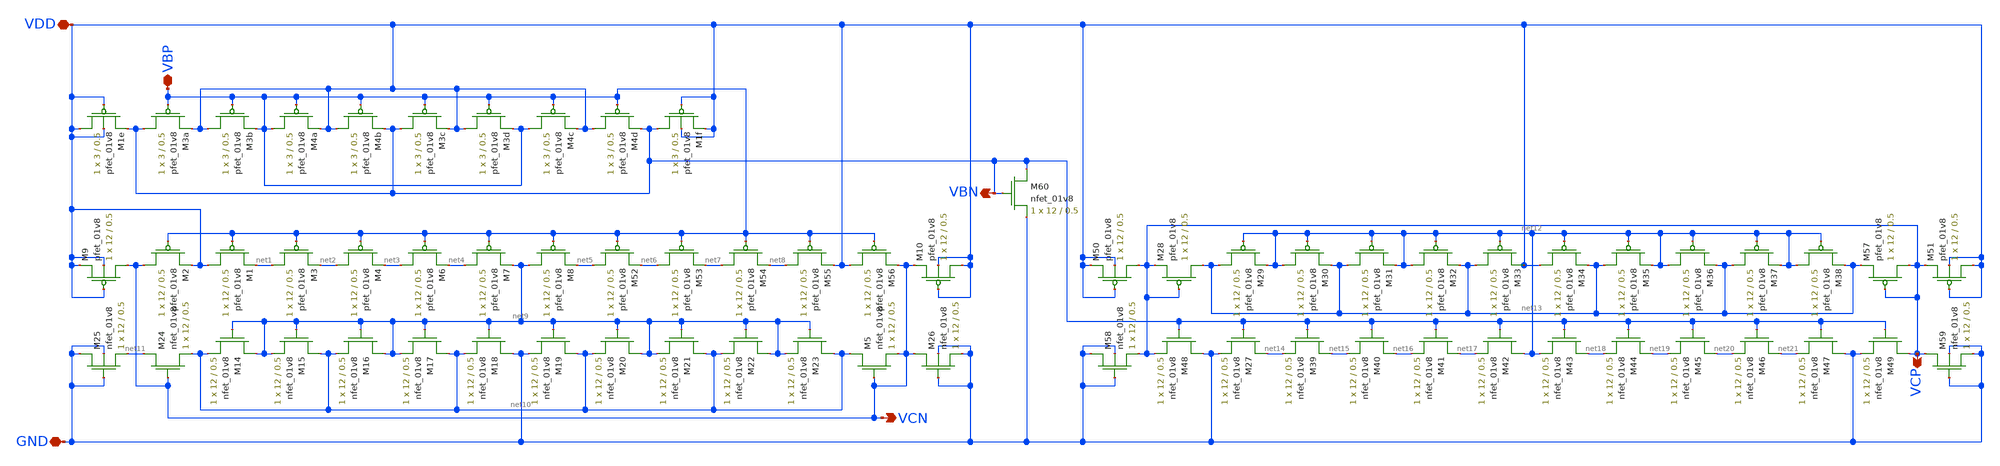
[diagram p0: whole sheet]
** sch_path: mp3/schematics/bias_generator_lds.sch
**.subckt bias_generator_lds VBP VDD GND VCN VCP VBN
*.iopin VBP
*.iopin VDD
*.iopin GND
*.opin VCN
*.opin VCP
*.opin VBN
XM9 VCN VDD VDD VDD sky130_fd_pr__pfet_01v8 L=0.5 W=12 nf=1 ad='int((nf+1)/2) * W/nf * 0.29' as='int((nf+2)/2) * W/nf * 0.29'
+ pd='2*int((nf+1)/2) * (W/nf + 0.29)' ps='2*int((nf+2)/2) * (W/nf + 0.29)' nrd='0.29 / W' nrs='0.29 / W'
+ sa=0 sb=0 sd=0 mult=1 m=1
XM24 net11 VCN net10 GND sky130_fd_pr__nfet_01v8 L=0.5 W=12 nf=1 ad='int((nf+1)/2) * W/nf * 0.29' as='int((nf+2)/2) * W/nf * 0.29'
+ pd='2*int((nf+1)/2) * (W/nf + 0.29)' ps='2*int((nf+2)/2) * (W/nf + 0.29)' nrd='0.29 / W' nrs='0.29 / W'
+ sa=0 sb=0 sd=0 mult=1 m=1
XM2 VCN VBP VDD VDD sky130_fd_pr__pfet_01v8 L=0.5 W=12 nf=1 ad='int((nf+1)/2) * W/nf * 0.29' as='int((nf+2)/2) * W/nf * 0.29'
+ pd='2*int((nf+1)/2) * (W/nf + 0.29)' ps='2*int((nf+2)/2) * (W/nf + 0.29)' nrd='0.29 / W' nrs='0.29 / W'
+ sa=0 sb=0 sd=0 mult=1 m=1
XM1 VDD VBP net1 VDD sky130_fd_pr__pfet_01v8 L=0.5 W=12 nf=1 ad='int((nf+1)/2) * W/nf * 0.29' as='int((nf+2)/2) * W/nf * 0.29'
+ pd='2*int((nf+1)/2) * (W/nf + 0.29)' ps='2*int((nf+2)/2) * (W/nf + 0.29)' nrd='0.29 / W' nrs='0.29 / W'
+ sa=0 sb=0 sd=0 mult=1 m=1
XM3 net1 VBP net2 VDD sky130_fd_pr__pfet_01v8 L=0.5 W=12 nf=1 ad='int((nf+1)/2) * W/nf * 0.29' as='int((nf+2)/2) * W/nf * 0.29'
+ pd='2*int((nf+1)/2) * (W/nf + 0.29)' ps='2*int((nf+2)/2) * (W/nf + 0.29)' nrd='0.29 / W' nrs='0.29 / W'
+ sa=0 sb=0 sd=0 mult=1 m=1
XM4 net2 VBP net3 VDD sky130_fd_pr__pfet_01v8 L=0.5 W=12 nf=1 ad='int((nf+1)/2) * W/nf * 0.29' as='int((nf+2)/2) * W/nf * 0.29'
+ pd='2*int((nf+1)/2) * (W/nf + 0.29)' ps='2*int((nf+2)/2) * (W/nf + 0.29)' nrd='0.29 / W' nrs='0.29 / W'
+ sa=0 sb=0 sd=0 mult=1 m=1
XM6 net3 VBP net4 VDD sky130_fd_pr__pfet_01v8 L=0.5 W=12 nf=1 ad='int((nf+1)/2) * W/nf * 0.29' as='int((nf+2)/2) * W/nf * 0.29'
+ pd='2*int((nf+1)/2) * (W/nf + 0.29)' ps='2*int((nf+2)/2) * (W/nf + 0.29)' nrd='0.29 / W' nrs='0.29 / W'
+ sa=0 sb=0 sd=0 mult=1 m=1
XM7 net4 VBP net9 VDD sky130_fd_pr__pfet_01v8 L=0.5 W=12 nf=1 ad='int((nf+1)/2) * W/nf * 0.29' as='int((nf+2)/2) * W/nf * 0.29'
+ pd='2*int((nf+1)/2) * (W/nf + 0.29)' ps='2*int((nf+2)/2) * (W/nf + 0.29)' nrd='0.29 / W' nrs='0.29 / W'
+ sa=0 sb=0 sd=0 mult=1 m=1
XM8 net9 VBP net5 VDD sky130_fd_pr__pfet_01v8 L=0.5 W=12 nf=1 ad='int((nf+1)/2) * W/nf * 0.29' as='int((nf+2)/2) * W/nf * 0.29'
+ pd='2*int((nf+1)/2) * (W/nf + 0.29)' ps='2*int((nf+2)/2) * (W/nf + 0.29)' nrd='0.29 / W' nrs='0.29 / W'
+ sa=0 sb=0 sd=0 mult=1 m=1
XM52 net5 VBP net6 VDD sky130_fd_pr__pfet_01v8 L=0.5 W=12 nf=1 ad='int((nf+1)/2) * W/nf * 0.29' as='int((nf+2)/2) * W/nf * 0.29'
+ pd='2*int((nf+1)/2) * (W/nf + 0.29)' ps='2*int((nf+2)/2) * (W/nf + 0.29)' nrd='0.29 / W' nrs='0.29 / W'
+ sa=0 sb=0 sd=0 mult=1 m=1
XM53 net6 VBP net7 VDD sky130_fd_pr__pfet_01v8 L=0.5 W=12 nf=1 ad='int((nf+1)/2) * W/nf * 0.29' as='int((nf+2)/2) * W/nf * 0.29'
+ pd='2*int((nf+1)/2) * (W/nf + 0.29)' ps='2*int((nf+2)/2) * (W/nf + 0.29)' nrd='0.29 / W' nrs='0.29 / W'
+ sa=0 sb=0 sd=0 mult=1 m=1
XM54 net7 VBP net8 VDD sky130_fd_pr__pfet_01v8 L=0.5 W=12 nf=1 ad='int((nf+1)/2) * W/nf * 0.29' as='int((nf+2)/2) * W/nf * 0.29'
+ pd='2*int((nf+1)/2) * (W/nf + 0.29)' ps='2*int((nf+2)/2) * (W/nf + 0.29)' nrd='0.29 / W' nrs='0.29 / W'
+ sa=0 sb=0 sd=0 mult=1 m=1
XM55 net8 VBP VDD VDD sky130_fd_pr__pfet_01v8 L=0.5 W=12 nf=1 ad='int((nf+1)/2) * W/nf * 0.29' as='int((nf+2)/2) * W/nf * 0.29'
+ pd='2*int((nf+1)/2) * (W/nf + 0.29)' ps='2*int((nf+2)/2) * (W/nf + 0.29)' nrd='0.29 / W' nrs='0.29 / W'
+ sa=0 sb=0 sd=0 mult=1 m=1
XM56 VDD VBP VCN VDD sky130_fd_pr__pfet_01v8 L=0.5 W=12 nf=1 ad='int((nf+1)/2) * W/nf * 0.29' as='int((nf+2)/2) * W/nf * 0.29'
+ pd='2*int((nf+1)/2) * (W/nf + 0.29)' ps='2*int((nf+2)/2) * (W/nf + 0.29)' nrd='0.29 / W' nrs='0.29 / W'
+ sa=0 sb=0 sd=0 mult=1 m=1
XM10 VDD VDD VCN VDD sky130_fd_pr__pfet_01v8 L=0.5 W=12 nf=1 ad='int((nf+1)/2) * W/nf * 0.29' as='int((nf+2)/2) * W/nf * 0.29'
+ pd='2*int((nf+1)/2) * (W/nf + 0.29)' ps='2*int((nf+2)/2) * (W/nf + 0.29)' nrd='0.29 / W' nrs='0.29 / W'
+ sa=0 sb=0 sd=0 mult=1 m=1
XM25 GND GND net11 GND sky130_fd_pr__nfet_01v8 L=0.5 W=12 nf=1 ad='int((nf+1)/2) * W/nf * 0.29' as='int((nf+2)/2) * W/nf * 0.29'
+ pd='2*int((nf+1)/2) * (W/nf + 0.29)' ps='2*int((nf+2)/2) * (W/nf + 0.29)' nrd='0.29 / W' nrs='0.29 / W'
+ sa=0 sb=0 sd=0 mult=1 m=1
XM14 net9 net9 net10 GND sky130_fd_pr__nfet_01v8 L=0.5 W=12 nf=1 ad='int((nf+1)/2) * W/nf * 0.29' as='int((nf+2)/2) * W/nf * 0.29'
+ pd='2*int((nf+1)/2) * (W/nf + 0.29)' ps='2*int((nf+2)/2) * (W/nf + 0.29)' nrd='0.29 / W' nrs='0.29 / W'
+ sa=0 sb=0 sd=0 mult=1 m=1
XM15 net10 net9 net9 GND sky130_fd_pr__nfet_01v8 L=0.5 W=12 nf=1 ad='int((nf+1)/2) * W/nf * 0.29' as='int((nf+2)/2) * W/nf * 0.29'
+ pd='2*int((nf+1)/2) * (W/nf + 0.29)' ps='2*int((nf+2)/2) * (W/nf + 0.29)' nrd='0.29 / W' nrs='0.29 / W'
+ sa=0 sb=0 sd=0 mult=1 m=1
XM16 net9 net9 net10 GND sky130_fd_pr__nfet_01v8 L=0.5 W=12 nf=1 ad='int((nf+1)/2) * W/nf * 0.29' as='int((nf+2)/2) * W/nf * 0.29'
+ pd='2*int((nf+1)/2) * (W/nf + 0.29)' ps='2*int((nf+2)/2) * (W/nf + 0.29)' nrd='0.29 / W' nrs='0.29 / W'
+ sa=0 sb=0 sd=0 mult=1 m=1
XM17 net10 net9 net9 GND sky130_fd_pr__nfet_01v8 L=0.5 W=12 nf=1 ad='int((nf+1)/2) * W/nf * 0.29' as='int((nf+2)/2) * W/nf * 0.29'
+ pd='2*int((nf+1)/2) * (W/nf + 0.29)' ps='2*int((nf+2)/2) * (W/nf + 0.29)' nrd='0.29 / W' nrs='0.29 / W'
+ sa=0 sb=0 sd=0 mult=1 m=1
XM18 GND net9 net10 GND sky130_fd_pr__nfet_01v8 L=0.5 W=12 nf=1 ad='int((nf+1)/2) * W/nf * 0.29' as='int((nf+2)/2) * W/nf * 0.29'
+ pd='2*int((nf+1)/2) * (W/nf + 0.29)' ps='2*int((nf+2)/2) * (W/nf + 0.29)' nrd='0.29 / W' nrs='0.29 / W'
+ sa=0 sb=0 sd=0 mult=1 m=1
XM19 net10 net9 GND GND sky130_fd_pr__nfet_01v8 L=0.5 W=12 nf=1 ad='int((nf+1)/2) * W/nf * 0.29' as='int((nf+2)/2) * W/nf * 0.29'
+ pd='2*int((nf+1)/2) * (W/nf + 0.29)' ps='2*int((nf+2)/2) * (W/nf + 0.29)' nrd='0.29 / W' nrs='0.29 / W'
+ sa=0 sb=0 sd=0 mult=1 m=1
XM20 net9 net9 net10 GND sky130_fd_pr__nfet_01v8 L=0.5 W=12 nf=1 ad='int((nf+1)/2) * W/nf * 0.29' as='int((nf+2)/2) * W/nf * 0.29'
+ pd='2*int((nf+1)/2) * (W/nf + 0.29)' ps='2*int((nf+2)/2) * (W/nf + 0.29)' nrd='0.29 / W' nrs='0.29 / W'
+ sa=0 sb=0 sd=0 mult=1 m=1
XM21 net10 net9 net9 GND sky130_fd_pr__nfet_01v8 L=0.5 W=12 nf=1 ad='int((nf+1)/2) * W/nf * 0.29' as='int((nf+2)/2) * W/nf * 0.29'
+ pd='2*int((nf+1)/2) * (W/nf + 0.29)' ps='2*int((nf+2)/2) * (W/nf + 0.29)' nrd='0.29 / W' nrs='0.29 / W'
+ sa=0 sb=0 sd=0 mult=1 m=1
XM22 net9 net9 net10 GND sky130_fd_pr__nfet_01v8 L=0.5 W=12 nf=1 ad='int((nf+1)/2) * W/nf * 0.29' as='int((nf+2)/2) * W/nf * 0.29'
+ pd='2*int((nf+1)/2) * (W/nf + 0.29)' ps='2*int((nf+2)/2) * (W/nf + 0.29)' nrd='0.29 / W' nrs='0.29 / W'
+ sa=0 sb=0 sd=0 mult=1 m=1
XM23 net10 net9 net9 GND sky130_fd_pr__nfet_01v8 L=0.5 W=12 nf=1 ad='int((nf+1)/2) * W/nf * 0.29' as='int((nf+2)/2) * W/nf * 0.29'
+ pd='2*int((nf+1)/2) * (W/nf + 0.29)' ps='2*int((nf+2)/2) * (W/nf + 0.29)' nrd='0.29 / W' nrs='0.29 / W'
+ sa=0 sb=0 sd=0 mult=1 m=1
XM5 net10 VCN VCN GND sky130_fd_pr__nfet_01v8 L=0.5 W=12 nf=1 ad='int((nf+1)/2) * W/nf * 0.29' as='int((nf+2)/2) * W/nf * 0.29'
+ pd='2*int((nf+1)/2) * (W/nf + 0.29)' ps='2*int((nf+2)/2) * (W/nf + 0.29)' nrd='0.29 / W' nrs='0.29 / W'
+ sa=0 sb=0 sd=0 mult=1 m=1
XM26 VCN GND GND GND sky130_fd_pr__nfet_01v8 L=0.5 W=12 nf=1 ad='int((nf+1)/2) * W/nf * 0.29' as='int((nf+2)/2) * W/nf * 0.29'
+ pd='2*int((nf+1)/2) * (W/nf + 0.29)' ps='2*int((nf+2)/2) * (W/nf + 0.29)' nrd='0.29 / W' nrs='0.29 / W'
+ sa=0 sb=0 sd=0 mult=1 m=1
XM27 net14 VBN GND GND sky130_fd_pr__nfet_01v8 L=0.5 W=12 nf=1 ad='int((nf+1)/2) * W/nf * 0.29' as='int((nf+2)/2) * W/nf * 0.29'
+ pd='2*int((nf+1)/2) * (W/nf + 0.29)' ps='2*int((nf+2)/2) * (W/nf + 0.29)' nrd='0.29 / W' nrs='0.29 / W'
+ sa=0 sb=0 sd=0 mult=1 m=1
XM39 net15 VBN net14 GND sky130_fd_pr__nfet_01v8 L=0.5 W=12 nf=1 ad='int((nf+1)/2) * W/nf * 0.29' as='int((nf+2)/2) * W/nf * 0.29'
+ pd='2*int((nf+1)/2) * (W/nf + 0.29)' ps='2*int((nf+2)/2) * (W/nf + 0.29)' nrd='0.29 / W' nrs='0.29 / W'
+ sa=0 sb=0 sd=0 mult=1 m=1
XM40 net16 VBN net15 GND sky130_fd_pr__nfet_01v8 L=0.5 W=12 nf=1 ad='int((nf+1)/2) * W/nf * 0.29' as='int((nf+2)/2) * W/nf * 0.29'
+ pd='2*int((nf+1)/2) * (W/nf + 0.29)' ps='2*int((nf+2)/2) * (W/nf + 0.29)' nrd='0.29 / W' nrs='0.29 / W'
+ sa=0 sb=0 sd=0 mult=1 m=1
XM41 net17 VBN net16 GND sky130_fd_pr__nfet_01v8 L=0.5 W=12 nf=1 ad='int((nf+1)/2) * W/nf * 0.29' as='int((nf+2)/2) * W/nf * 0.29'
+ pd='2*int((nf+1)/2) * (W/nf + 0.29)' ps='2*int((nf+2)/2) * (W/nf + 0.29)' nrd='0.29 / W' nrs='0.29 / W'
+ sa=0 sb=0 sd=0 mult=1 m=1
XM42 net12 VBN net17 GND sky130_fd_pr__nfet_01v8 L=0.5 W=12 nf=1 ad='int((nf+1)/2) * W/nf * 0.29' as='int((nf+2)/2) * W/nf * 0.29'
+ pd='2*int((nf+1)/2) * (W/nf + 0.29)' ps='2*int((nf+2)/2) * (W/nf + 0.29)' nrd='0.29 / W' nrs='0.29 / W'
+ sa=0 sb=0 sd=0 mult=1 m=1
XM43 net18 VBN net12 GND sky130_fd_pr__nfet_01v8 L=0.5 W=12 nf=1 ad='int((nf+1)/2) * W/nf * 0.29' as='int((nf+2)/2) * W/nf * 0.29'
+ pd='2*int((nf+1)/2) * (W/nf + 0.29)' ps='2*int((nf+2)/2) * (W/nf + 0.29)' nrd='0.29 / W' nrs='0.29 / W'
+ sa=0 sb=0 sd=0 mult=1 m=1
XM44 net19 VBN net18 GND sky130_fd_pr__nfet_01v8 L=0.5 W=12 nf=1 ad='int((nf+1)/2) * W/nf * 0.29' as='int((nf+2)/2) * W/nf * 0.29'
+ pd='2*int((nf+1)/2) * (W/nf + 0.29)' ps='2*int((nf+2)/2) * (W/nf + 0.29)' nrd='0.29 / W' nrs='0.29 / W'
+ sa=0 sb=0 sd=0 mult=1 m=1
XM45 net20 VBN net19 GND sky130_fd_pr__nfet_01v8 L=0.5 W=12 nf=1 ad='int((nf+1)/2) * W/nf * 0.29' as='int((nf+2)/2) * W/nf * 0.29'
+ pd='2*int((nf+1)/2) * (W/nf + 0.29)' ps='2*int((nf+2)/2) * (W/nf + 0.29)' nrd='0.29 / W' nrs='0.29 / W'
+ sa=0 sb=0 sd=0 mult=1 m=1
XM46 net21 VBN net20 GND sky130_fd_pr__nfet_01v8 L=0.5 W=12 nf=1 ad='int((nf+1)/2) * W/nf * 0.29' as='int((nf+2)/2) * W/nf * 0.29'
+ pd='2*int((nf+1)/2) * (W/nf + 0.29)' ps='2*int((nf+2)/2) * (W/nf + 0.29)' nrd='0.29 / W' nrs='0.29 / W'
+ sa=0 sb=0 sd=0 mult=1 m=1
XM47 GND VBN net21 GND sky130_fd_pr__nfet_01v8 L=0.5 W=12 nf=1 ad='int((nf+1)/2) * W/nf * 0.29' as='int((nf+2)/2) * W/nf * 0.29'
+ pd='2*int((nf+1)/2) * (W/nf + 0.29)' ps='2*int((nf+2)/2) * (W/nf + 0.29)' nrd='0.29 / W' nrs='0.29 / W'
+ sa=0 sb=0 sd=0 mult=1 m=1
XM48 GND VBN VCP GND sky130_fd_pr__nfet_01v8 L=0.5 W=12 nf=1 ad='int((nf+1)/2) * W/nf * 0.29' as='int((nf+2)/2) * W/nf * 0.29'
+ pd='2*int((nf+1)/2) * (W/nf + 0.29)' ps='2*int((nf+2)/2) * (W/nf + 0.29)' nrd='0.29 / W' nrs='0.29 / W'
+ sa=0 sb=0 sd=0 mult=1 m=1
XM49 VCP VBN GND GND sky130_fd_pr__nfet_01v8 L=0.5 W=12 nf=1 ad='int((nf+1)/2) * W/nf * 0.29' as='int((nf+2)/2) * W/nf * 0.29'
+ pd='2*int((nf+1)/2) * (W/nf + 0.29)' ps='2*int((nf+2)/2) * (W/nf + 0.29)' nrd='0.29 / W' nrs='0.29 / W'
+ sa=0 sb=0 sd=0 mult=1 m=1
XM29 net13 net12 net12 VDD sky130_fd_pr__pfet_01v8 L=0.5 W=12 nf=1 ad='int((nf+1)/2) * W/nf * 0.29' as='int((nf+2)/2) * W/nf * 0.29'
+ pd='2*int((nf+1)/2) * (W/nf + 0.29)' ps='2*int((nf+2)/2) * (W/nf + 0.29)' nrd='0.29 / W' nrs='0.29 / W'
+ sa=0 sb=0 sd=0 mult=1 m=1
XM30 net12 net12 net13 VDD sky130_fd_pr__pfet_01v8 L=0.5 W=12 nf=1 ad='int((nf+1)/2) * W/nf * 0.29' as='int((nf+2)/2) * W/nf * 0.29'
+ pd='2*int((nf+1)/2) * (W/nf + 0.29)' ps='2*int((nf+2)/2) * (W/nf + 0.29)' nrd='0.29 / W' nrs='0.29 / W'
+ sa=0 sb=0 sd=0 mult=1 m=1
XM31 net13 net12 net12 VDD sky130_fd_pr__pfet_01v8 L=0.5 W=12 nf=1 ad='int((nf+1)/2) * W/nf * 0.29' as='int((nf+2)/2) * W/nf * 0.29'
+ pd='2*int((nf+1)/2) * (W/nf + 0.29)' ps='2*int((nf+2)/2) * (W/nf + 0.29)' nrd='0.29 / W' nrs='0.29 / W'
+ sa=0 sb=0 sd=0 mult=1 m=1
XM32 net12 net12 net13 VDD sky130_fd_pr__pfet_01v8 L=0.5 W=12 nf=1 ad='int((nf+1)/2) * W/nf * 0.29' as='int((nf+2)/2) * W/nf * 0.29'
+ pd='2*int((nf+1)/2) * (W/nf + 0.29)' ps='2*int((nf+2)/2) * (W/nf + 0.29)' nrd='0.29 / W' nrs='0.29 / W'
+ sa=0 sb=0 sd=0 mult=1 m=1
XM33 net13 net12 VDD VDD sky130_fd_pr__pfet_01v8 L=0.5 W=12 nf=1 ad='int((nf+1)/2) * W/nf * 0.29' as='int((nf+2)/2) * W/nf * 0.29'
+ pd='2*int((nf+1)/2) * (W/nf + 0.29)' ps='2*int((nf+2)/2) * (W/nf + 0.29)' nrd='0.29 / W' nrs='0.29 / W'
+ sa=0 sb=0 sd=0 mult=1 m=1
XM34 VDD net12 net13 VDD sky130_fd_pr__pfet_01v8 L=0.5 W=12 nf=1 ad='int((nf+1)/2) * W/nf * 0.29' as='int((nf+2)/2) * W/nf * 0.29'
+ pd='2*int((nf+1)/2) * (W/nf + 0.29)' ps='2*int((nf+2)/2) * (W/nf + 0.29)' nrd='0.29 / W' nrs='0.29 / W'
+ sa=0 sb=0 sd=0 mult=1 m=1
XM35 net13 net12 net12 VDD sky130_fd_pr__pfet_01v8 L=0.5 W=12 nf=1 ad='int((nf+1)/2) * W/nf * 0.29' as='int((nf+2)/2) * W/nf * 0.29'
+ pd='2*int((nf+1)/2) * (W/nf + 0.29)' ps='2*int((nf+2)/2) * (W/nf + 0.29)' nrd='0.29 / W' nrs='0.29 / W'
+ sa=0 sb=0 sd=0 mult=1 m=1
XM36 net12 net12 net13 VDD sky130_fd_pr__pfet_01v8 L=0.5 W=12 nf=1 ad='int((nf+1)/2) * W/nf * 0.29' as='int((nf+2)/2) * W/nf * 0.29'
+ pd='2*int((nf+1)/2) * (W/nf + 0.29)' ps='2*int((nf+2)/2) * (W/nf + 0.29)' nrd='0.29 / W' nrs='0.29 / W'
+ sa=0 sb=0 sd=0 mult=1 m=1
XM37 net13 net12 net12 VDD sky130_fd_pr__pfet_01v8 L=0.5 W=12 nf=1 ad='int((nf+1)/2) * W/nf * 0.29' as='int((nf+2)/2) * W/nf * 0.29'
+ pd='2*int((nf+1)/2) * (W/nf + 0.29)' ps='2*int((nf+2)/2) * (W/nf + 0.29)' nrd='0.29 / W' nrs='0.29 / W'
+ sa=0 sb=0 sd=0 mult=1 m=1
XM38 net12 net12 net13 VDD sky130_fd_pr__pfet_01v8 L=0.5 W=12 nf=1 ad='int((nf+1)/2) * W/nf * 0.29' as='int((nf+2)/2) * W/nf * 0.29'
+ pd='2*int((nf+1)/2) * (W/nf + 0.29)' ps='2*int((nf+2)/2) * (W/nf + 0.29)' nrd='0.29 / W' nrs='0.29 / W'
+ sa=0 sb=0 sd=0 mult=1 m=1
XM57 VCP VCP net13 VDD sky130_fd_pr__pfet_01v8 L=0.5 W=12 nf=1 ad='int((nf+1)/2) * W/nf * 0.29' as='int((nf+2)/2) * W/nf * 0.29'
+ pd='2*int((nf+1)/2) * (W/nf + 0.29)' ps='2*int((nf+2)/2) * (W/nf + 0.29)' nrd='0.29 / W' nrs='0.29 / W'
+ sa=0 sb=0 sd=0 mult=1 m=1
XM28 net13 VCP VCP VDD sky130_fd_pr__pfet_01v8 L=0.5 W=12 nf=1 ad='int((nf+1)/2) * W/nf * 0.29' as='int((nf+2)/2) * W/nf * 0.29'
+ pd='2*int((nf+1)/2) * (W/nf + 0.29)' ps='2*int((nf+2)/2) * (W/nf + 0.29)' nrd='0.29 / W' nrs='0.29 / W'
+ sa=0 sb=0 sd=0 mult=1 m=1
XM50 VCP VDD VDD VDD sky130_fd_pr__pfet_01v8 L=0.5 W=12 nf=1 ad='int((nf+1)/2) * W/nf * 0.29' as='int((nf+2)/2) * W/nf * 0.29'
+ pd='2*int((nf+1)/2) * (W/nf + 0.29)' ps='2*int((nf+2)/2) * (W/nf + 0.29)' nrd='0.29 / W' nrs='0.29 / W'
+ sa=0 sb=0 sd=0 mult=1 m=1
XM51 VDD VDD VCP VDD sky130_fd_pr__pfet_01v8 L=0.5 W=12 nf=1 ad='int((nf+1)/2) * W/nf * 0.29' as='int((nf+2)/2) * W/nf * 0.29'
+ pd='2*int((nf+1)/2) * (W/nf + 0.29)' ps='2*int((nf+2)/2) * (W/nf + 0.29)' nrd='0.29 / W' nrs='0.29 / W'
+ sa=0 sb=0 sd=0 mult=1 m=1
XM58 GND GND VCP GND sky130_fd_pr__nfet_01v8 L=0.5 W=12 nf=1 ad='int((nf+1)/2) * W/nf * 0.29' as='int((nf+2)/2) * W/nf * 0.29'
+ pd='2*int((nf+1)/2) * (W/nf + 0.29)' ps='2*int((nf+2)/2) * (W/nf + 0.29)' nrd='0.29 / W' nrs='0.29 / W'
+ sa=0 sb=0 sd=0 mult=1 m=1
XM59 VCP GND GND GND sky130_fd_pr__nfet_01v8 L=0.5 W=12 nf=1 ad='int((nf+1)/2) * W/nf * 0.29' as='int((nf+2)/2) * W/nf * 0.29'
+ pd='2*int((nf+1)/2) * (W/nf + 0.29)' ps='2*int((nf+2)/2) * (W/nf + 0.29)' nrd='0.29 / W' nrs='0.29 / W'
+ sa=0 sb=0 sd=0 mult=1 m=1
XM3b VDD VBP VBP VDD sky130_fd_pr__pfet_01v8 L=0.5 W=3 nf=1 ad='int((nf+1)/2) * W/nf * 0.29' as='int((nf+2)/2) * W/nf * 0.29'
+ pd='2*int((nf+1)/2) * (W/nf + 0.29)' ps='2*int((nf+2)/2) * (W/nf + 0.29)' nrd='0.29 / W' nrs='0.29 / W'
+ sa=0 sb=0 sd=0 mult=1 m=1
XM3a VBN VBP VDD VDD sky130_fd_pr__pfet_01v8 L=0.5 W=3 nf=1 ad='int((nf+1)/2) * W/nf * 0.29' as='int((nf+2)/2) * W/nf * 0.29'
+ pd='2*int((nf+1)/2) * (W/nf + 0.29)' ps='2*int((nf+2)/2) * (W/nf + 0.29)' nrd='0.29 / W' nrs='0.29 / W'
+ sa=0 sb=0 sd=0 mult=1 m=1
XM4a VBP VBP VDD VDD sky130_fd_pr__pfet_01v8 L=0.5 W=3 nf=1 ad='int((nf+1)/2) * W/nf * 0.29' as='int((nf+2)/2) * W/nf * 0.29'
+ pd='2*int((nf+1)/2) * (W/nf + 0.29)' ps='2*int((nf+2)/2) * (W/nf + 0.29)' nrd='0.29 / W' nrs='0.29 / W'
+ sa=0 sb=0 sd=0 mult=1 m=1
XM4b VDD VBP VBN VDD sky130_fd_pr__pfet_01v8 L=0.5 W=3 nf=1 ad='int((nf+1)/2) * W/nf * 0.29' as='int((nf+2)/2) * W/nf * 0.29'
+ pd='2*int((nf+1)/2) * (W/nf + 0.29)' ps='2*int((nf+2)/2) * (W/nf + 0.29)' nrd='0.29 / W' nrs='0.29 / W'
+ sa=0 sb=0 sd=0 mult=1 m=1
XM3c VBN VBP VDD VDD sky130_fd_pr__pfet_01v8 L=0.5 W=3 nf=1 ad='int((nf+1)/2) * W/nf * 0.29' as='int((nf+2)/2) * W/nf * 0.29'
+ pd='2*int((nf+1)/2) * (W/nf + 0.29)' ps='2*int((nf+2)/2) * (W/nf + 0.29)' nrd='0.29 / W' nrs='0.29 / W'
+ sa=0 sb=0 sd=0 mult=1 m=1
XM3d VDD VBP VBP VDD sky130_fd_pr__pfet_01v8 L=0.5 W=3 nf=1 ad='int((nf+1)/2) * W/nf * 0.29' as='int((nf+2)/2) * W/nf * 0.29'
+ pd='2*int((nf+1)/2) * (W/nf + 0.29)' ps='2*int((nf+2)/2) * (W/nf + 0.29)' nrd='0.29 / W' nrs='0.29 / W'
+ sa=0 sb=0 sd=0 mult=1 m=1
XM4c VBP VBP VDD VDD sky130_fd_pr__pfet_01v8 L=0.5 W=3 nf=1 ad='int((nf+1)/2) * W/nf * 0.29' as='int((nf+2)/2) * W/nf * 0.29'
+ pd='2*int((nf+1)/2) * (W/nf + 0.29)' ps='2*int((nf+2)/2) * (W/nf + 0.29)' nrd='0.29 / W' nrs='0.29 / W'
+ sa=0 sb=0 sd=0 mult=1 m=1
XM1e VDD VDD VBN VDD sky130_fd_pr__pfet_01v8 L=0.5 W=3 nf=1 ad='int((nf+1)/2) * W/nf * 0.29' as='int((nf+2)/2) * W/nf * 0.29'
+ pd='2*int((nf+1)/2) * (W/nf + 0.29)' ps='2*int((nf+2)/2) * (W/nf + 0.29)' nrd='0.29 / W' nrs='0.29 / W'
+ sa=0 sb=0 sd=0 mult=1 m=1
XM1f VBN VDD VDD VDD sky130_fd_pr__pfet_01v8 L=0.5 W=3 nf=1 ad='int((nf+1)/2) * W/nf * 0.29' as='int((nf+2)/2) * W/nf * 0.29'
+ pd='2*int((nf+1)/2) * (W/nf + 0.29)' ps='2*int((nf+2)/2) * (W/nf + 0.29)' nrd='0.29 / W' nrs='0.29 / W'
+ sa=0 sb=0 sd=0 mult=1 m=1
XM4d VDD VBP VBN VDD sky130_fd_pr__pfet_01v8 L=0.5 W=3 nf=1 ad='int((nf+1)/2) * W/nf * 0.29' as='int((nf+2)/2) * W/nf * 0.29'
+ pd='2*int((nf+1)/2) * (W/nf + 0.29)' ps='2*int((nf+2)/2) * (W/nf + 0.29)' nrd='0.29 / W' nrs='0.29 / W'
+ sa=0 sb=0 sd=0 mult=1 m=1
XM60 VBN VBN GND GND sky130_fd_pr__nfet_01v8 L=0.5 W=12 nf=1 ad='int((nf+1)/2) * W/nf * 0.29' as='int((nf+2)/2) * W/nf * 0.29'
+ pd='2*int((nf+1)/2) * (W/nf + 0.29)' ps='2*int((nf+2)/2) * (W/nf + 0.29)' nrd='0.29 / W' nrs='0.29 / W'
+ sa=0 sb=0 sd=0 mult=1 m=1
**.ends
.end
